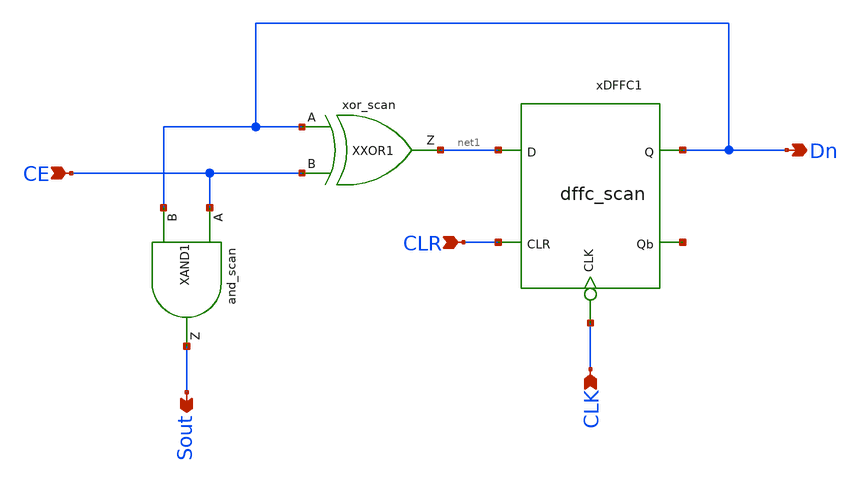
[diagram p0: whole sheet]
** sch_path: xschem/counter1b.sch
**.subckt counter1b CE CLR CLK Dn Sout
*.ipin CE
*.ipin CLR
*.ipin CLK
*.opin Dn
*.opin Sout
xDFFC1 Dn net1 CLK CLR net2 VSS VDD dffc_scan
XXOR1 Dn CE net1 VSS VDD xor_scan
XAND1 CE Dn Sout VSS VDD and_scan
**.ends
.end
